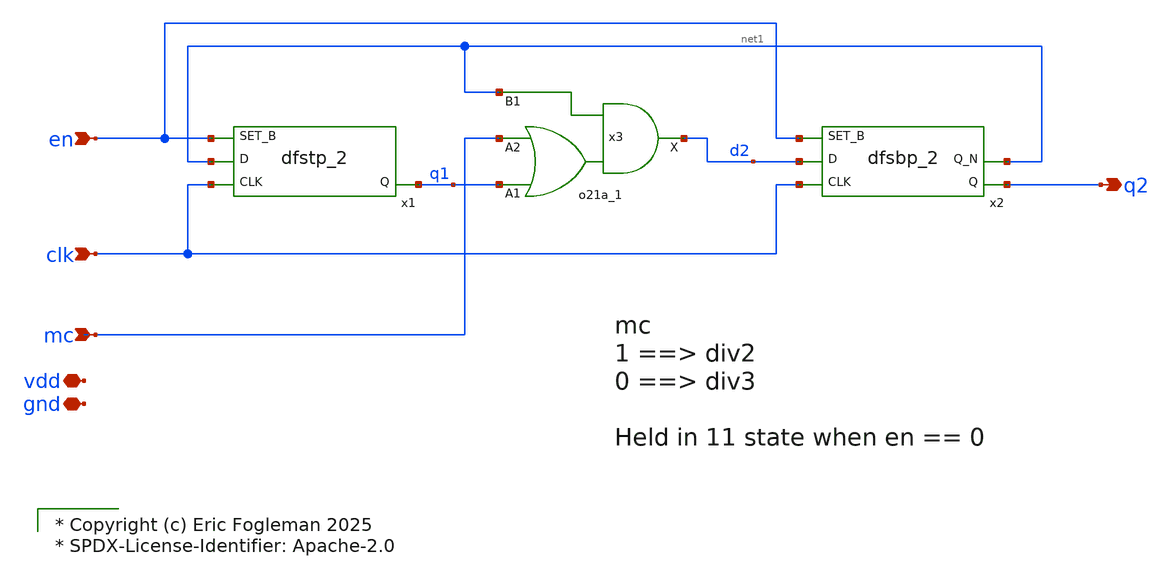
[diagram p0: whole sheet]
** sch_path: xschem/ejf_pll96_div23.sch

* Copyright (c) Eric Fogleman 2025
* SPDX-License-Identifier: Apache-2.0

**.subckt ejf_pll96_div23 clk mc q2 vdd gnd en
*.ipin clk
*.ipin mc
*.opin q2
*.iopin vdd
*.iopin gnd
*.ipin en
x3 q1 mc net1 gnd gnd vdd vdd d2 sky130_fd_sc_ls__o21a_1
x1 clk net1 en gnd gnd vdd vdd q1 sky130_fd_sc_ls__dfstp_2
x2 clk d2 en gnd gnd vdd vdd q2 net1 sky130_fd_sc_ls__dfsbp_2
**.ends
.end
